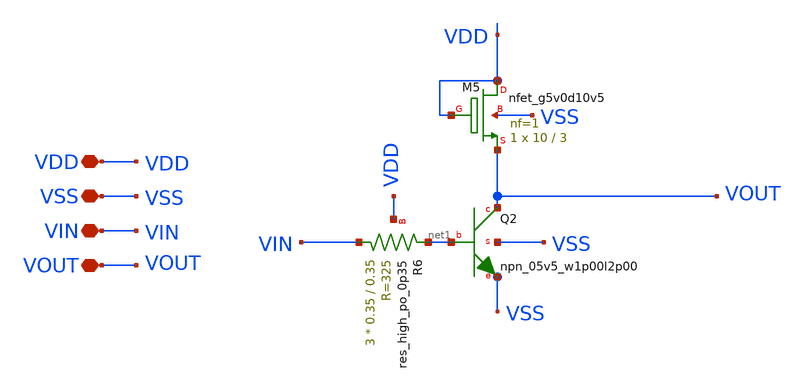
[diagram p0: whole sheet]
** sch_path: amplifiers/single_stage_amps/basic_stages/ce_diode_nmos_stage/ce_diode_nmos_stage.sch
**.subckt ce_diode_nmos_stage VDD VSS VIN VOUT
*.iopin VDD
*.iopin VSS
*.iopin VIN
*.iopin VOUT
XR6 VIN net1 VDD sky130_fd_pr__res_high_po_0p35 L=0.35 mult=3 m=3
XQ2 VOUT net1 VSS VSS sky130_fd_pr__npn_05v5_w1p00l2p00
XM5 VDD VDD VOUT VSS sky130_fd_pr__nfet_g5v0d10v5 L=3 W=10 nf=1 ad='int((1 + 1)/2) * 10 / 1 * 0.29' as='int((1 + 2)/2) * 10 / 1 * 0.29'
+ pd='2*int((1 + 1)/2) * (10 / 1 + 0.29)' ps='2*int((1 + 2)/2) * (10 / 1 + 0.29)' nrd='0.29 / 10 ' nrs='0.29 / 10 '
+ sa=0 sb=0 sd=0 mult=1 m=1
**.ends
.end
